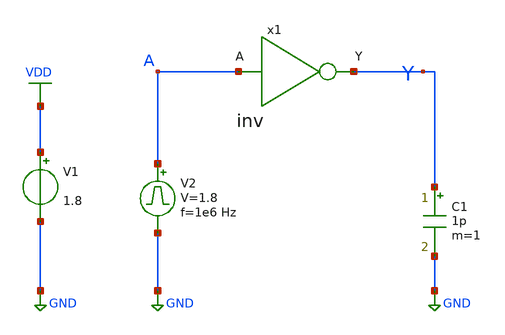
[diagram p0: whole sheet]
** sch_path: library/xschem/lab1/inv_tb.sch
**.subckt inv_tb
V1 VDD GND 1.8
V2 A GND pulse 0 1.8 '0.495/ 1e6 ' '0.01/1e6 ' '0.01/1e6 ' '0.49/1e6 ' '1/1e6 '
C1 Y GND 1p m=1
x1 Y A inv
**** begin user architecture code


.control
save all
tran 1n 2u
plot V(A) V(Y)+2
.endc



** opencircuitdesign pdks install
.lib $::SKYWATER_MODELS/sky130.lib.spice tt


**** end user architecture code
**.ends

* expanding   symbol:  lab1/inv.sym # of pins=2
** sym_path: library/xschem/lab1/inv.sym
** sch_path: library/xschem/lab1/inv.sch
.subckt inv Y A
*.ipin A
*.opin Y
XM1 Y A GND GND sky130_fd_pr__nfet_01v8 L=0.15 W=0.5 nf=1 ad='int((nf+1)/2) * W/nf * 0.29' as='int((nf+2)/2) * W/nf * 0.29'
+ pd='2*int((nf+1)/2) * (W/nf + 0.29)' ps='2*int((nf+2)/2) * (W/nf + 0.29)' nrd='0.29 / W' nrs='0.29 / W'
+ sa=0 sb=0 sd=0 mult=1 m=1
XM2 Y A VDD VDD sky130_fd_pr__pfet_01v8 L=0.15 W=1 nf=1 ad='int((nf+1)/2) * W/nf * 0.29' as='int((nf+2)/2) * W/nf * 0.29'
+ pd='2*int((nf+1)/2) * (W/nf + 0.29)' ps='2*int((nf+2)/2) * (W/nf + 0.29)' nrd='0.29 / W' nrs='0.29 / W'
+ sa=0 sb=0 sd=0 mult=1 m=1
.ends

.GLOBAL VDD
.GLOBAL GND
.end
